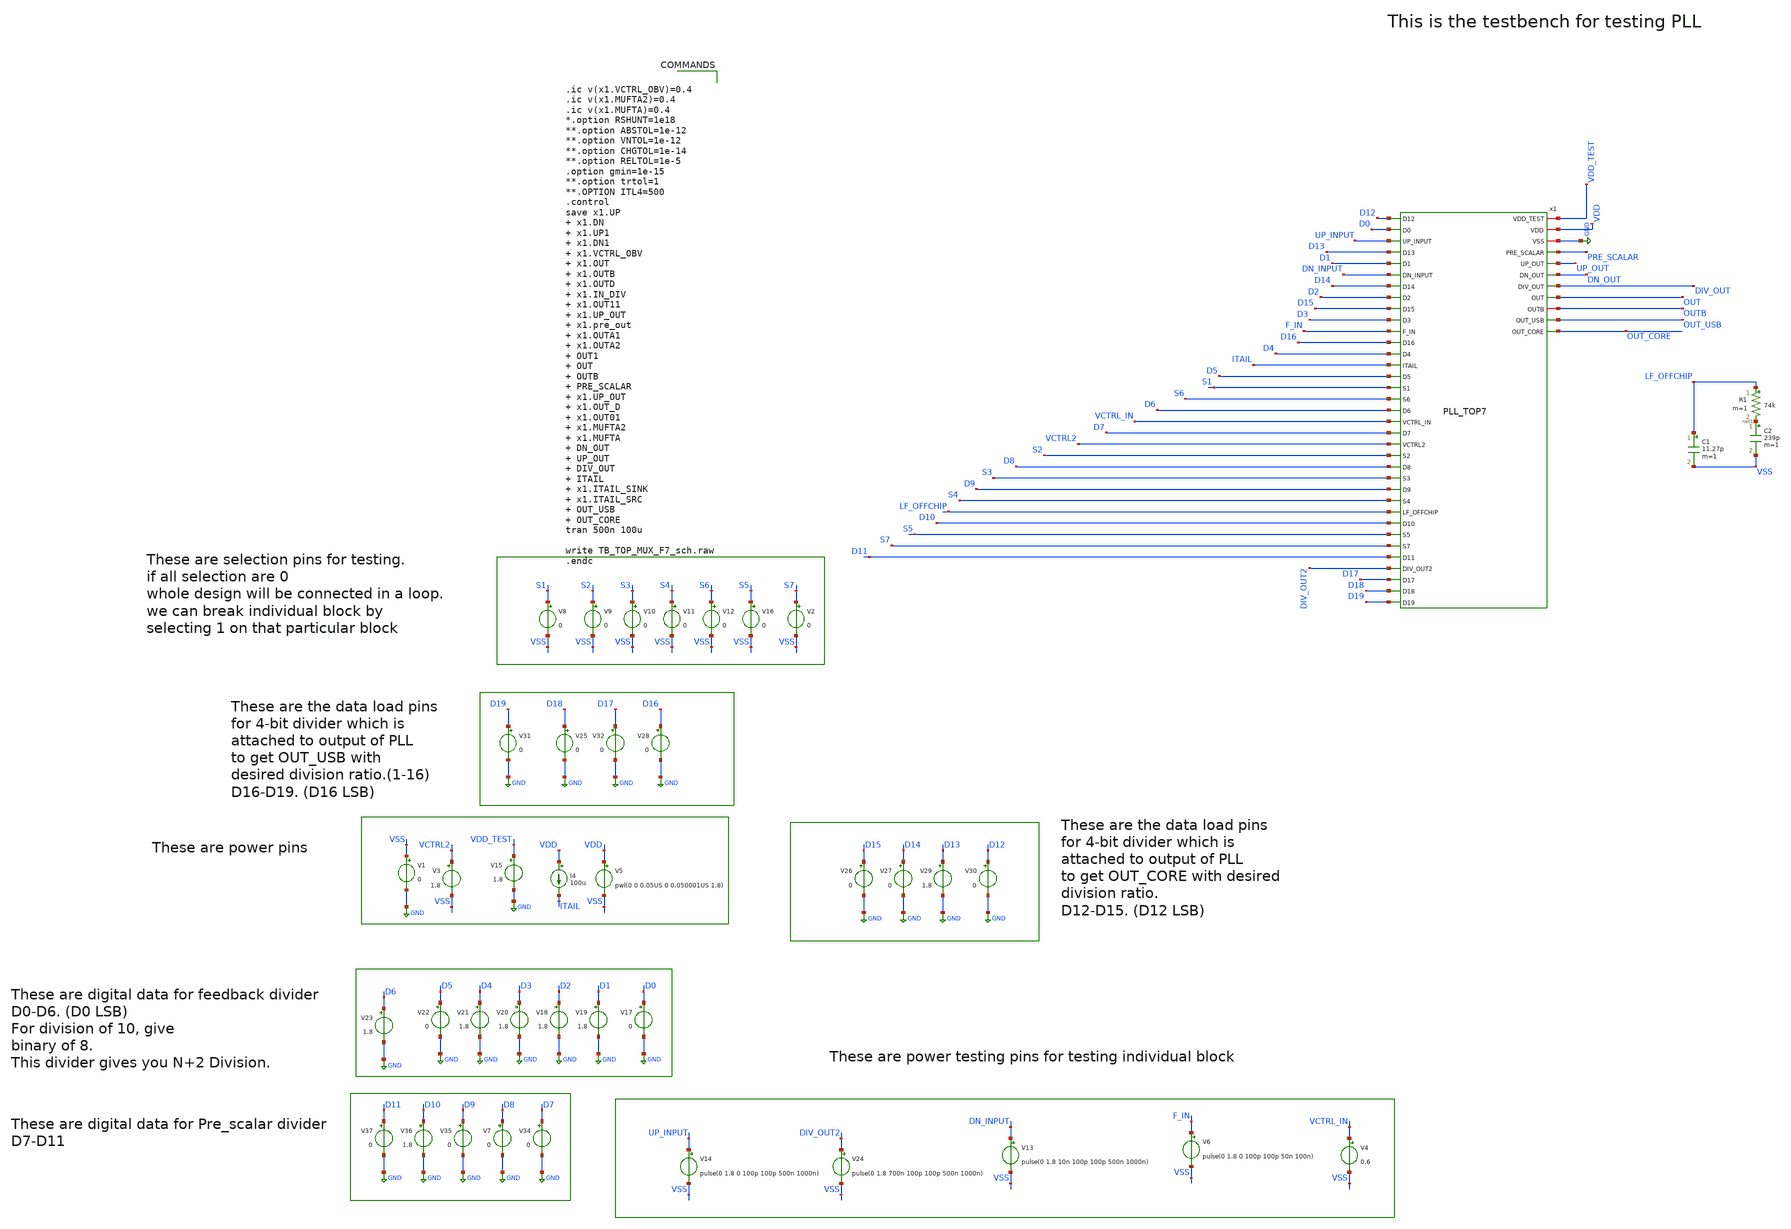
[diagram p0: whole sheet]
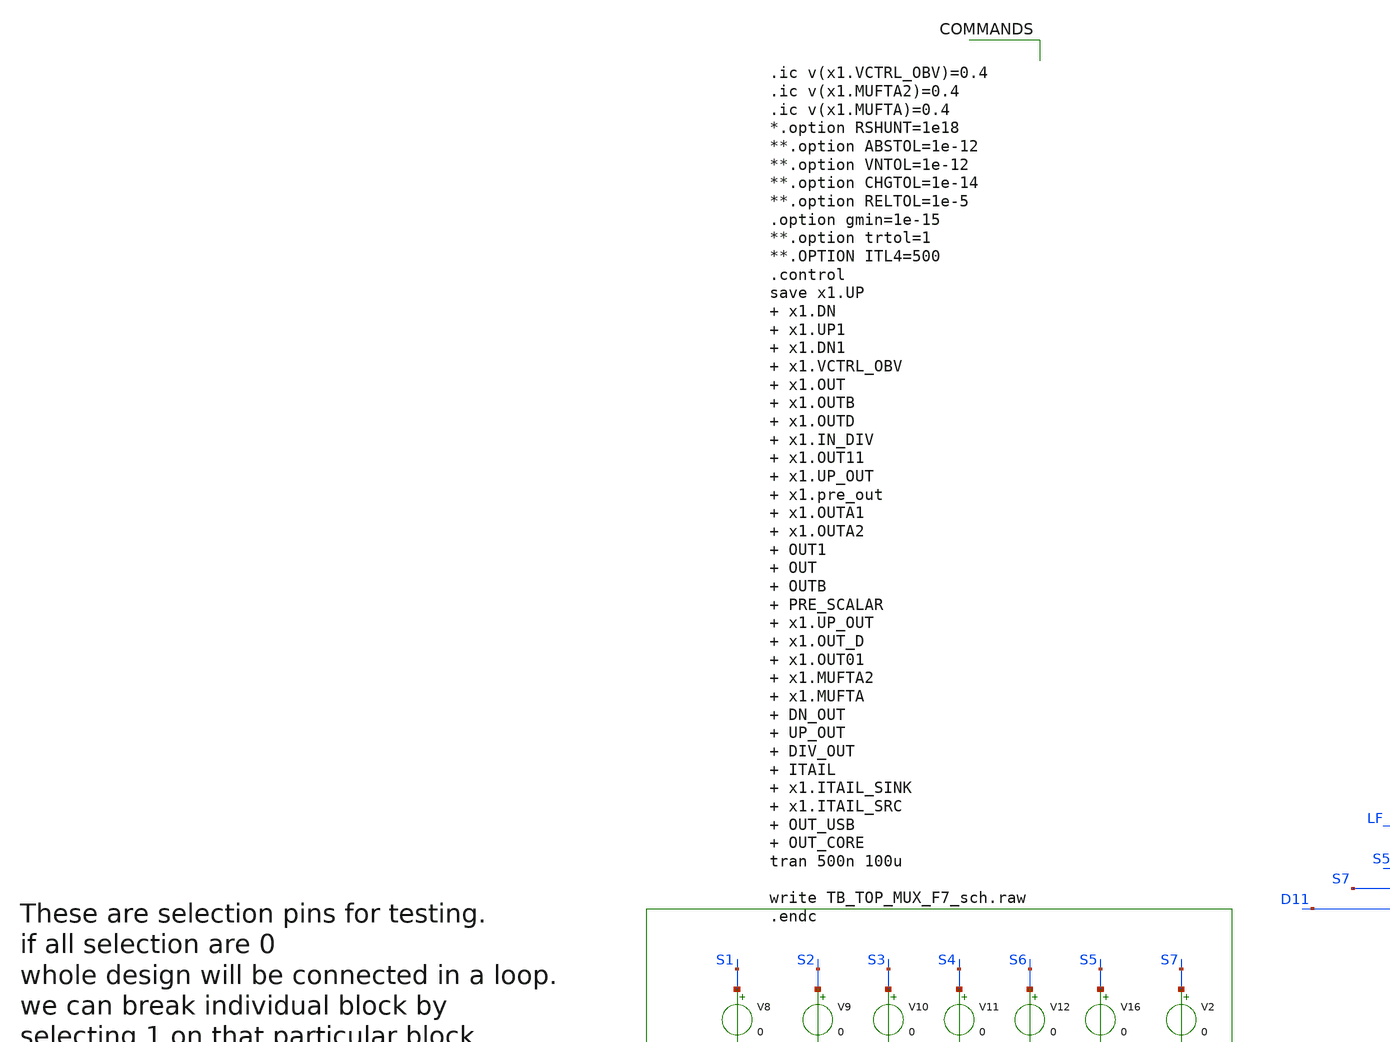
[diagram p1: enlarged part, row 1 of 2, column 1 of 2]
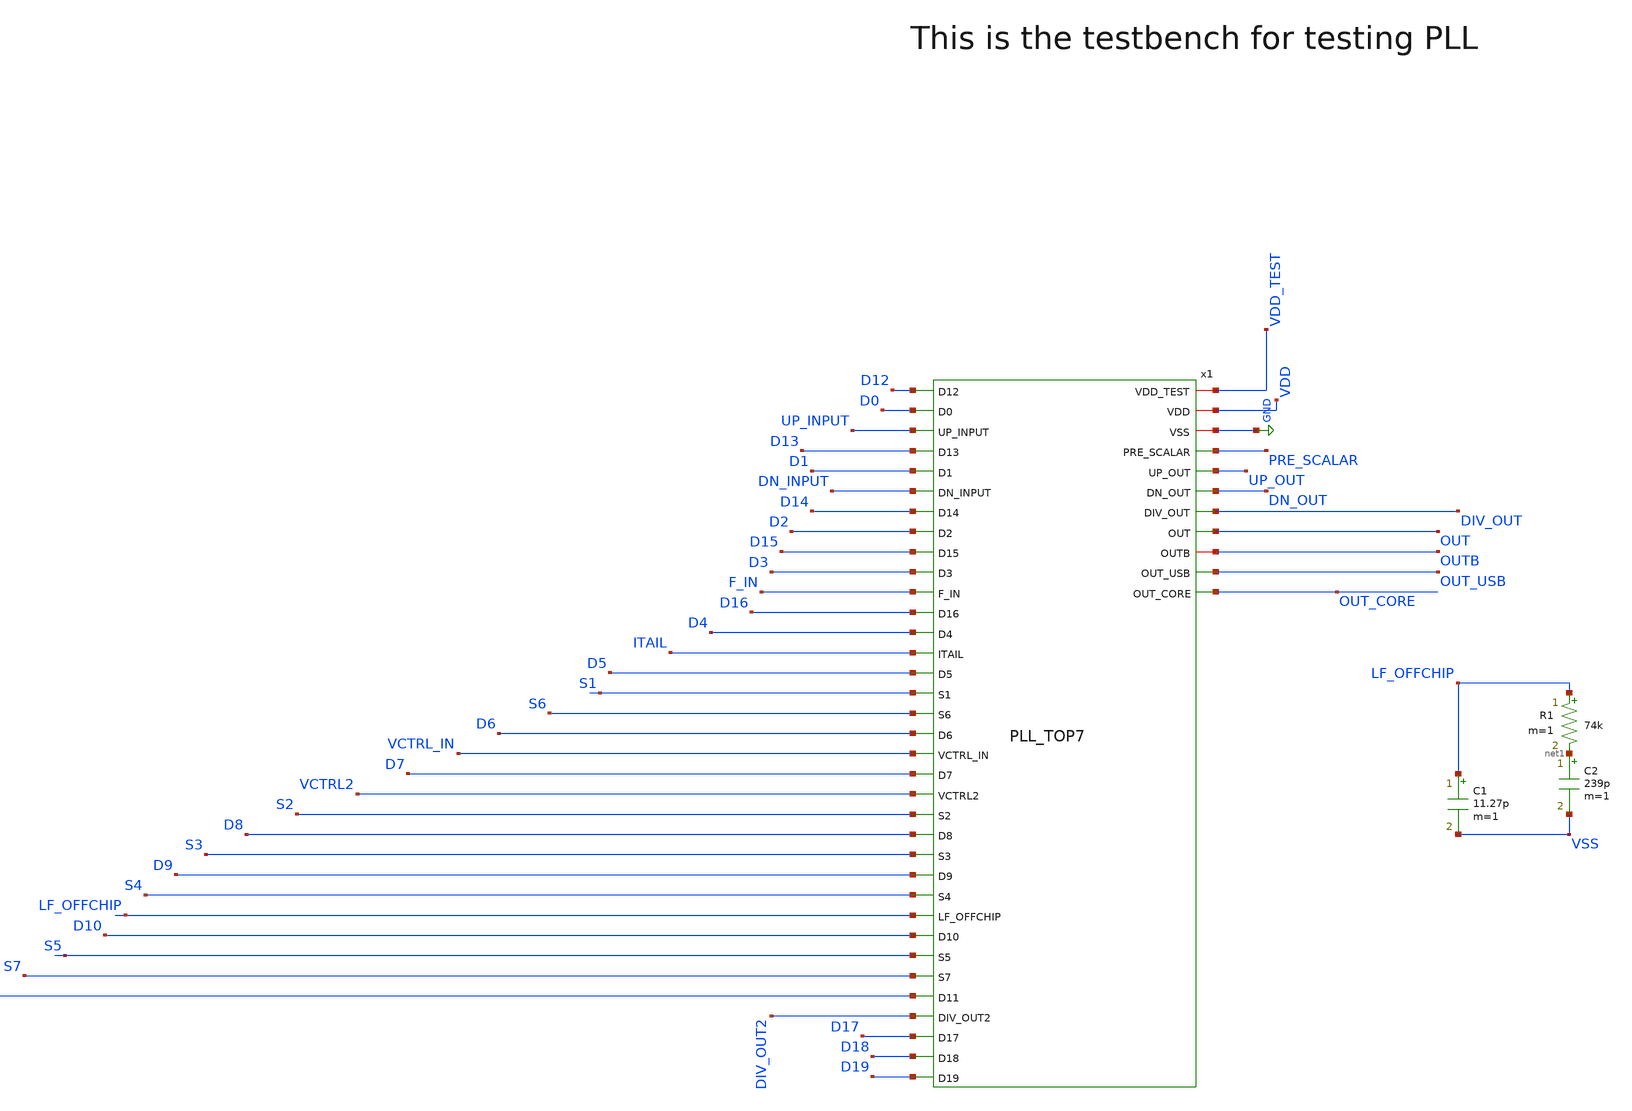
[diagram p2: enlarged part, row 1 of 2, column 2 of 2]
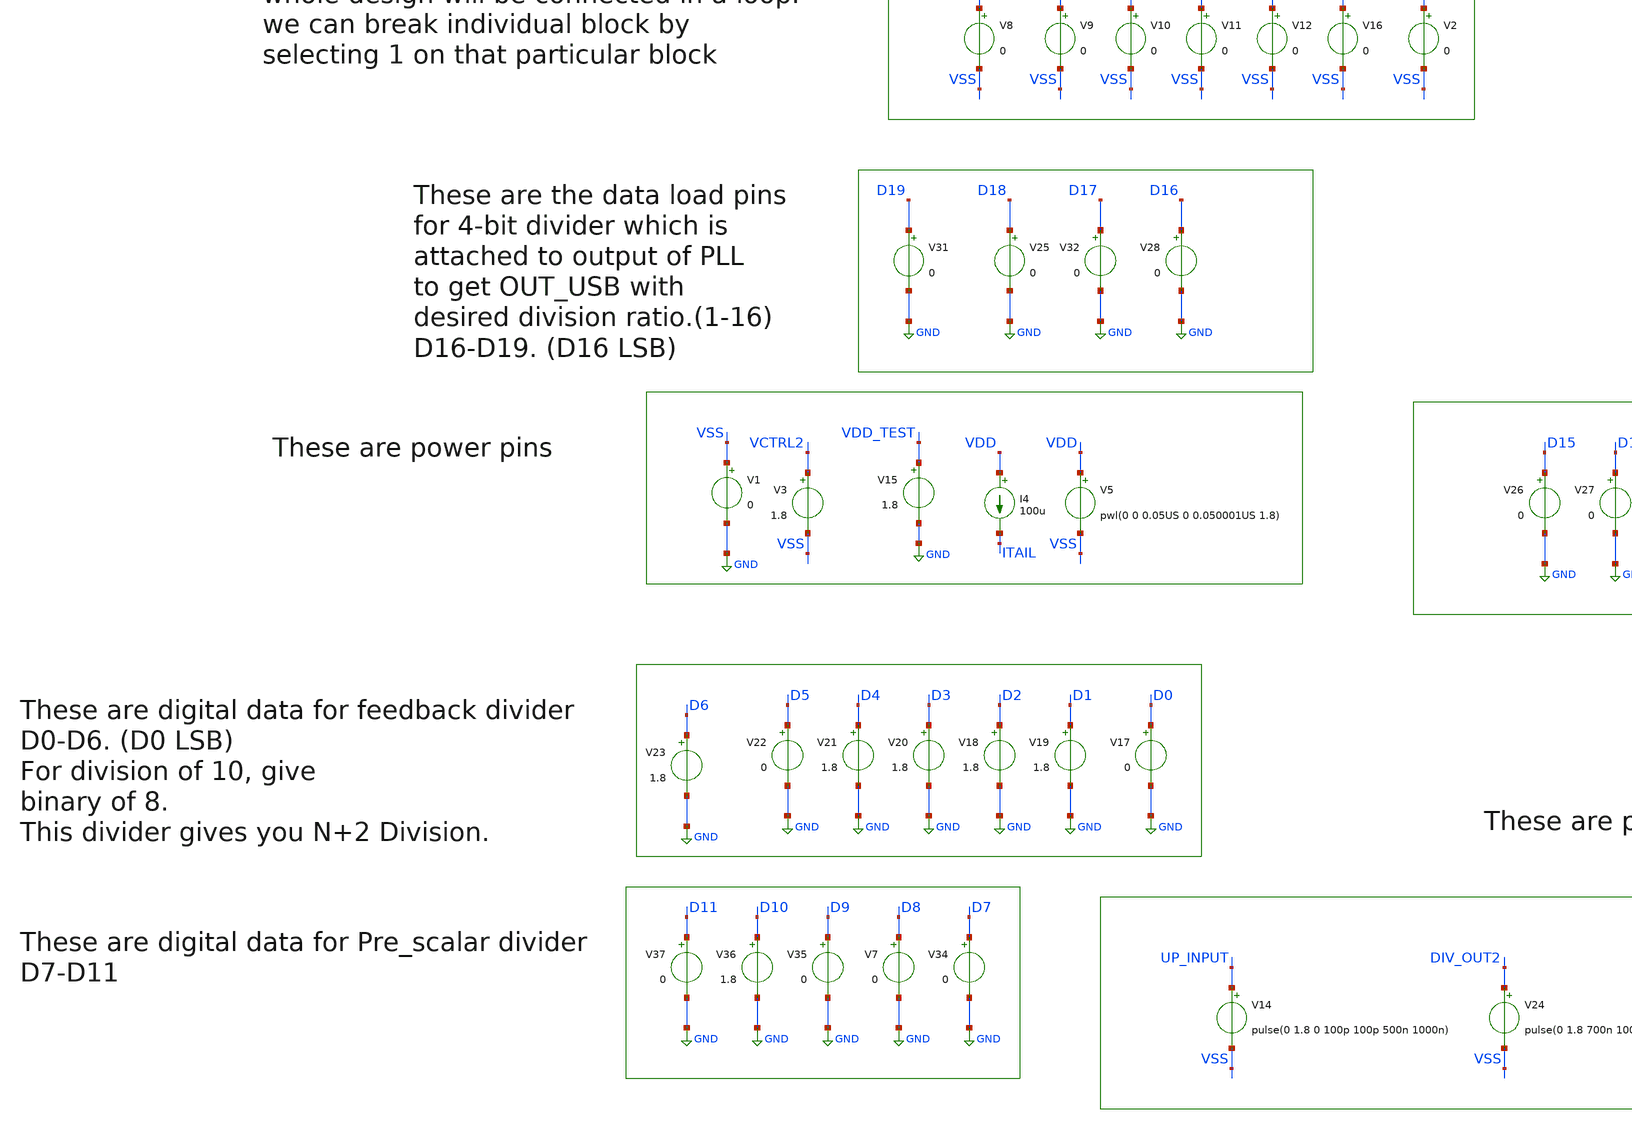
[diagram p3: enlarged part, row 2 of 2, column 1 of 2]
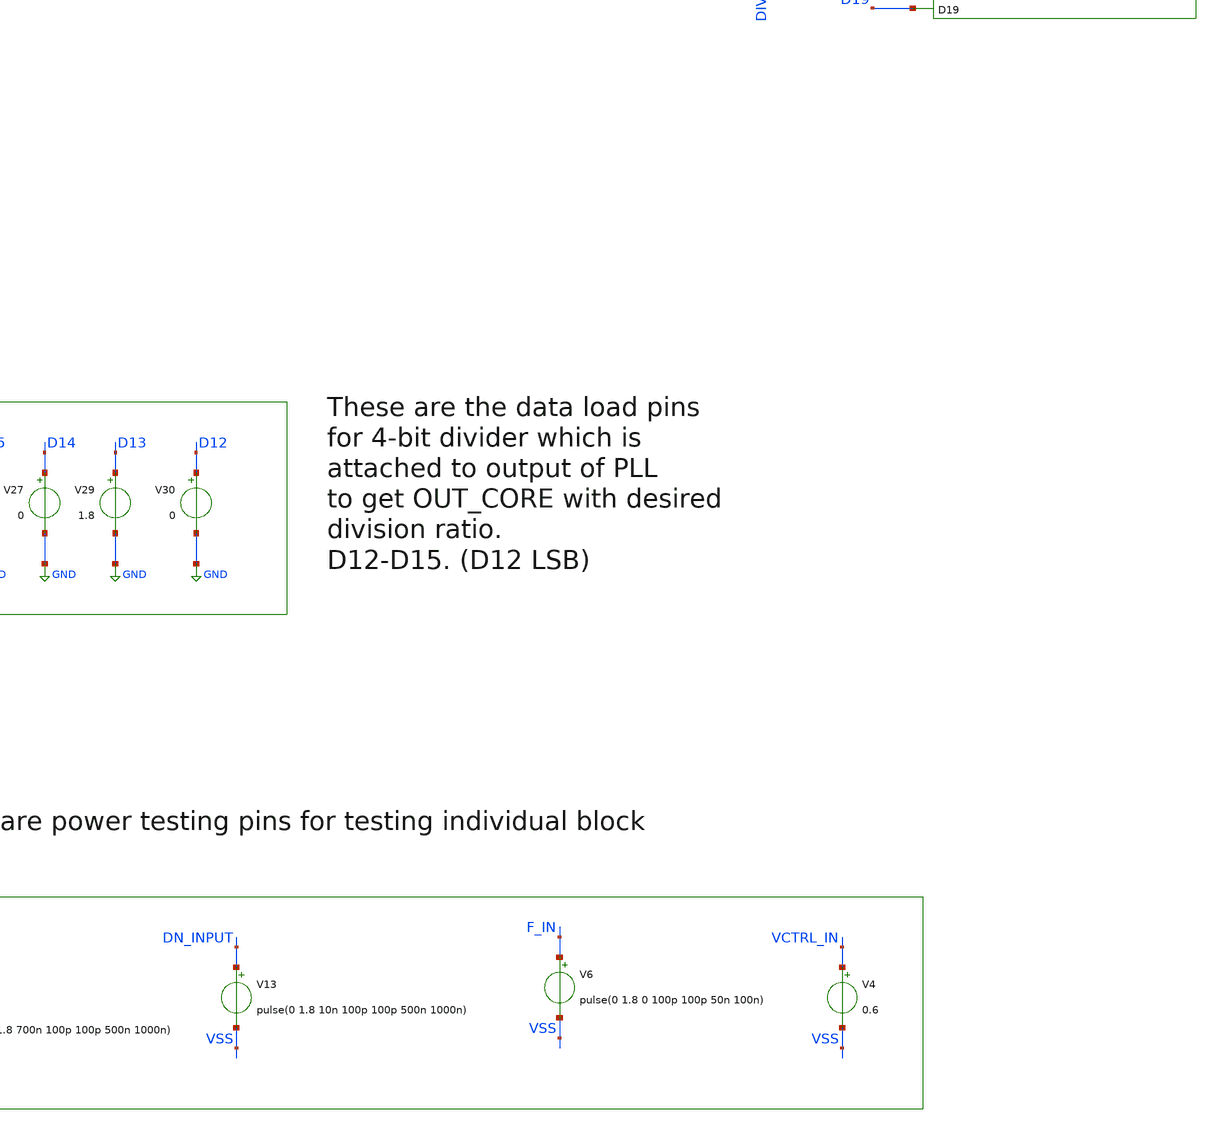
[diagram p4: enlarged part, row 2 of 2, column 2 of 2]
** sch_path: Xschem/PLL_TOP/TB_TOP_MUX_F7_sch.sch
**.subckt TB_TOP_MUX_F7_sch
V1 VSS GND 0
V4 VCTRL_IN VSS 0.6
V6 F_IN VSS pulse(0 1.8 0 100p 100p 50n 100n)
I4 VDD ITAIL 100u
V8 S1 VSS 0
V9 S2 VSS 0
V10 S3 VSS 0
V11 S4 VSS 0
V12 S6 VSS 0
V13 DN_INPUT VSS pulse(0 1.8 10n 100p 100p 500n 1000n)
V14 UP_INPUT VSS pulse(0 1.8 0 100p 100p 500n 1000n)
C1 LF_OFFCHIP VSS 11.27p m=1
R1 LF_OFFCHIP net1 74k m=1
C2 net1 VSS 239p m=1
V16 S5 VSS 0
V17 D0 GND 0
V2 S7 VSS 0
V5 VDD VSS pwl(0 0 0.05US 0 0.050001US 1.8)
V35 D9 GND 0
V37 D11 GND 0
V24 DIV_OUT2 VSS pulse(0 1.8 700n 100p 100p 500n 1000n)
V20 D3 GND 1.8
V22 D5 GND 0
V3 VCTRL2 VSS 1.8
V15 VDD_TEST GND 1.8
V36 D10 GND 1.8
V7 D8 GND 0
V34 D7 GND 0
V21 D4 GND 1.8
V23 D6 GND 1.8
x1 VDD_TEST D12 D0 VDD UP_INPUT D13 D1 DN_INPUT GND D14 D2 PRE_SCALAR UP_OUT D15 D3 F_IN DN_OUT D16
+ D4 ITAIL DIV_OUT D5 S1 S6 D6 VCTRL_IN D7 VCTRL2 S2 D8 S3 OUT D9 OUTB S4 LF_OFFCHIP D10 S5 S7 D11
+ OUT_USB DIV_OUT2 D17 OUT_CORE D18 D19 PLL_TOP7
V25 D18 GND 0
V26 D15 GND 0
V31 D19 GND 0
V28 D16 GND 0
V27 D14 GND 0
V29 D13 GND 1.8
V30 D12 GND 0
V32 D17 GND 0
V18 D2 GND 1.8
V19 D1 GND 1.8
**** begin user architecture code


.ic v(x1.VCTRL_OBV)=0.4
.ic v(x1.MUFTA2)=0.4
.ic v(x1.MUFTA)=0.4
*.option RSHUNT=1e18
**.option ABSTOL=1e-12
**.option VNTOL=1e-12
**.option CHGTOL=1e-14
**.option RELTOL=1e-5
.option gmin=1e-15
**.option trtol=1
**.OPTION ITL4=500
.control
save x1.UP  x1.DN  x1.UP1  x1.DN1  x1.VCTRL_OBV  x1.OUT  x1.OUTB  x1.OUTD  x1.IN_DIV  x1.OUT11
+  x1.UP_OUT  x1.pre_out  x1.OUTA1  x1.OUTA2  OUT1  OUT  OUTB  PRE_SCALAR  x1.UP_OUT  x1.OUT_D  x1.OUT01
+  x1.MUFTA2  x1.MUFTA  DN_OUT  UP_OUT  DIV_OUT  ITAIL  x1.ITAIL_SINK  x1.ITAIL_SRC  OUT_USB  OUT_CORE
tran 500n 100u

write TB_TOP_MUX_F7_sch.raw
.endc



** opencircuitdesign pdks install
.lib $::SKYWATER_MODELS/sky130.lib.spice ff


**** end user architecture code
**.ends
.GLOBAL GND
.end
